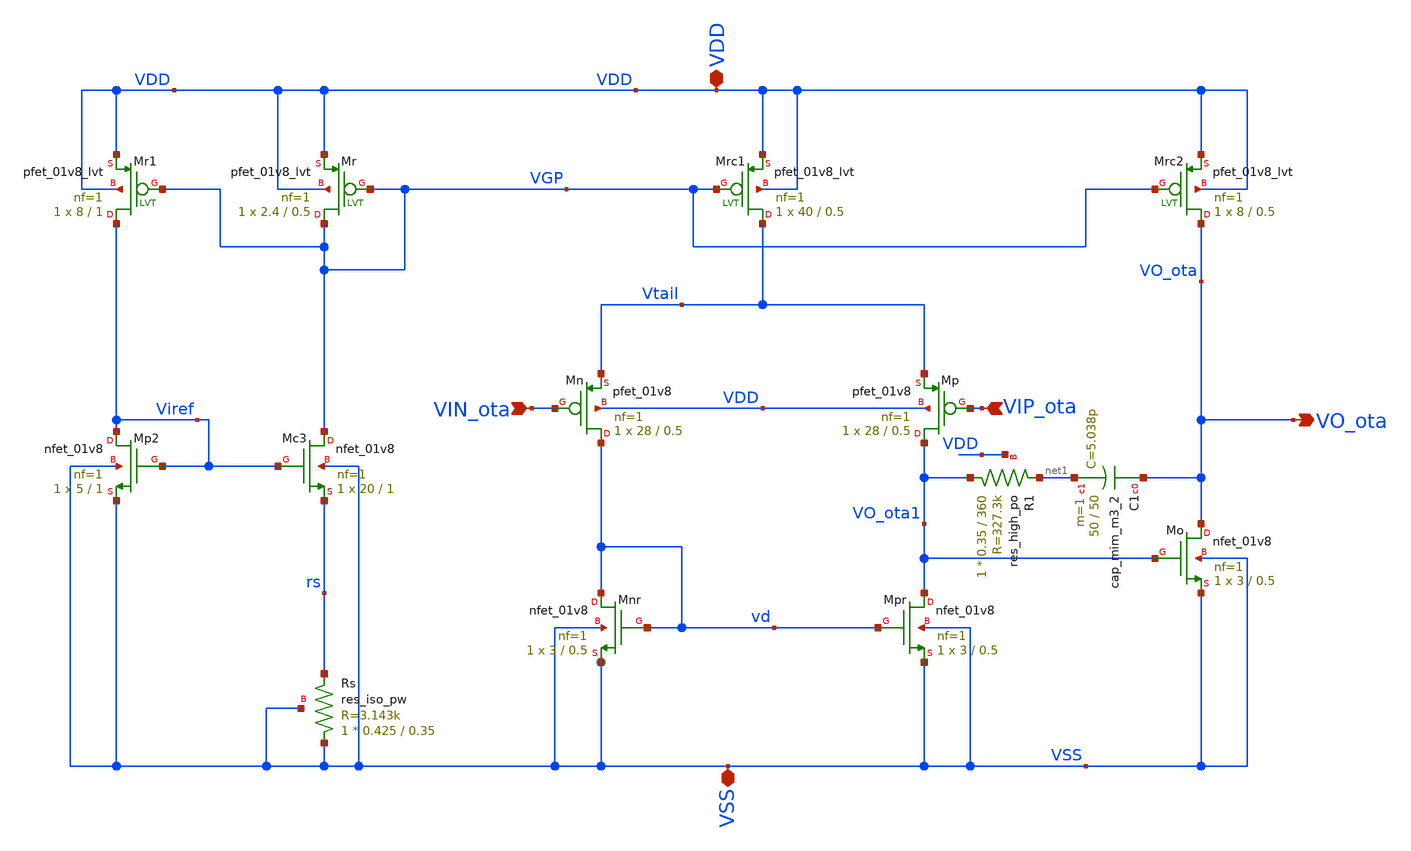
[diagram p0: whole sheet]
** sch_path: xschem/OTA.sch
**.subckt OTA VIN_ota VO_ota VSS VDD VIP_ota
*.ipin VIN_ota
*.opin VO_ota
*.iopin VSS
*.iopin VDD
*.ipin VIP_ota
XR1 VO_ota1 net1 VDD sky130_fd_pr__res_high_po W=0.35 L=360 mult=1 m=1
XC1 VO_ota net1 sky130_fd_pr__cap_mim_m3_2 W=50 L=50 MF=1 m=1
XMpr VO_ota1 vd VSS VSS sky130_fd_pr__nfet_01v8 L=0.5 W=3 nf=1 ad='int((1 + 1)/2) * 3 / 1 * 0.29' as='int((1 + 2)/2) * 3 / 1 * 0.29'
+ pd='2*int((1 + 1)/2) * (3 / 1 + 0.29)' ps='2*int((1 + 2)/2) * (3 / 1 + 0.29)' nrd='0.29 / 3 ' nrs='0.29 / 3 '
+ sa=0 sb=0 sd=0 mult=1 m=1
XMnr vd vd VSS VSS sky130_fd_pr__nfet_01v8 L=0.5 W=3 nf=1 ad='int((1 + 1)/2) * 3 / 1 * 0.29' as='int((1 + 2)/2) * 3 / 1 * 0.29'
+ pd='2*int((1 + 1)/2) * (3 / 1 + 0.29)' ps='2*int((1 + 2)/2) * (3 / 1 + 0.29)' nrd='0.29 / 3 ' nrs='0.29 / 3 '
+ sa=0 sb=0 sd=0 mult=1 m=1
XMn vd VIN_ota Vtail VDD sky130_fd_pr__pfet_01v8 L=0.5 W=28 nf=1 ad='int((1 + 1)/2) * 28 / 1 * 0.29'
+ as='int((1 + 2)/2) * 28 / 1 * 0.29' pd='2*int((1 + 1)/2) * (28 / 1 + 0.29)' ps='2*int((1 + 2)/2) * (28 / 1 + 0.29)'
+ nrd='0.29 / 28 ' nrs='0.29 / 28 ' sa=0 sb=0 sd=0 mult=1 m=1
XMp VO_ota1 VIP_ota Vtail VDD sky130_fd_pr__pfet_01v8 L=0.5 W=28 nf=1 ad='int((1 + 1)/2) * 28 / 1 * 0.29'
+ as='int((1 + 2)/2) * 28 / 1 * 0.29' pd='2*int((1 + 1)/2) * (28 / 1 + 0.29)' ps='2*int((1 + 2)/2) * (28 / 1 + 0.29)'
+ nrd='0.29 / 28 ' nrs='0.29 / 28 ' sa=0 sb=0 sd=0 mult=1 m=1
XMo VO_ota VO_ota1 VSS VSS sky130_fd_pr__nfet_01v8 L=0.5 W=3 nf=1 ad='int((1 + 1)/2) * 3 / 1 * 0.29'
+ as='int((1 + 2)/2) * 3 / 1 * 0.29' pd='2*int((1 + 1)/2) * (3 / 1 + 0.29)' ps='2*int((1 + 2)/2) * (3 / 1 + 0.29)'
+ nrd='0.29 / 3 ' nrs='0.29 / 3 ' sa=0 sb=0 sd=0 mult=1 m=1
XMrc1 Vtail VGP VDD VDD sky130_fd_pr__pfet_01v8_lvt L=0.5 W=40 nf=1 ad='int((1 + 1)/2) * 40 / 1 * 0.29'
+ as='int((1 + 2)/2) * 40 / 1 * 0.29' pd='2*int((1 + 1)/2) * (40 / 1 + 0.29)' ps='2*int((1 + 2)/2) * (40 / 1 + 0.29)'
+ nrd='0.29 / 40 ' nrs='0.29 / 40 ' sa=0 sb=0 sd=0 mult=1 m=1
XMrc2 VO_ota VGP VDD VDD sky130_fd_pr__pfet_01v8_lvt L=0.5 W=8 nf=1 ad='int((1 + 1)/2) * 8 / 1 * 0.29'
+ as='int((1 + 2)/2) * 8 / 1 * 0.29' pd='2*int((1 + 1)/2) * (8 / 1 + 0.29)' ps='2*int((1 + 2)/2) * (8 / 1 + 0.29)'
+ nrd='0.29 / 8 ' nrs='0.29 / 8 ' sa=0 sb=0 sd=0 mult=1 m=1
XMc3 VGP Viref rs VSS sky130_fd_pr__nfet_01v8 L=1 W=20 nf=1 ad='int((1 + 1)/2) * 20 / 1 * 0.29' as='int((1 + 2)/2) * 20 / 1 * 0.29'
+ pd='2*int((1 + 1)/2) * (20 / 1 + 0.29)' ps='2*int((1 + 2)/2) * (20 / 1 + 0.29)' nrd='0.29 / 20 ' nrs='0.29 / 20 '
+ sa=0 sb=0 sd=0 mult=1 m=1
XMp2 Viref Viref VSS VSS sky130_fd_pr__nfet_01v8 L=1 W=5 nf=1 ad='int((1 + 1)/2) * 5 / 1 * 0.29' as='int((1 + 2)/2) * 5 / 1 * 0.29'
+ pd='2*int((1 + 1)/2) * (5 / 1 + 0.29)' ps='2*int((1 + 2)/2) * (5 / 1 + 0.29)' nrd='0.29 / 5 ' nrs='0.29 / 5 '
+ sa=0 sb=0 sd=0 mult=1 m=1
XMr VGP VGP VDD VDD sky130_fd_pr__pfet_01v8_lvt L=0.5 W=2.4 nf=1 ad='int((1 + 1)/2) * 2.4 / 1 * 0.29'
+ as='int((1 + 2)/2) * 2.4 / 1 * 0.29' pd='2*int((1 + 1)/2) * (2.4 / 1 + 0.29)' ps='2*int((1 + 2)/2) * (2.4 / 1 + 0.29)'
+ nrd='0.29 / 2.4 ' nrs='0.29 / 2.4 ' sa=0 sb=0 sd=0 mult=1 m=1
XMr1 Viref VGP VDD VDD sky130_fd_pr__pfet_01v8_lvt L=1 W=8 nf=1 ad='int((1 + 1)/2) * 8 / 1 * 0.29' as='int((1 + 2)/2) * 8 / 1 * 0.29'
+ pd='2*int((1 + 1)/2) * (8 / 1 + 0.29)' ps='2*int((1 + 2)/2) * (8 / 1 + 0.29)' nrd='0.29 / 8 ' nrs='0.29 / 8 '
+ sa=0 sb=0 sd=0 mult=1 m=1
XRs VSS rs VSS sky130_fd_pr__res_iso_pw W=0.425 L=0.35 m=1
**.ends
.end
